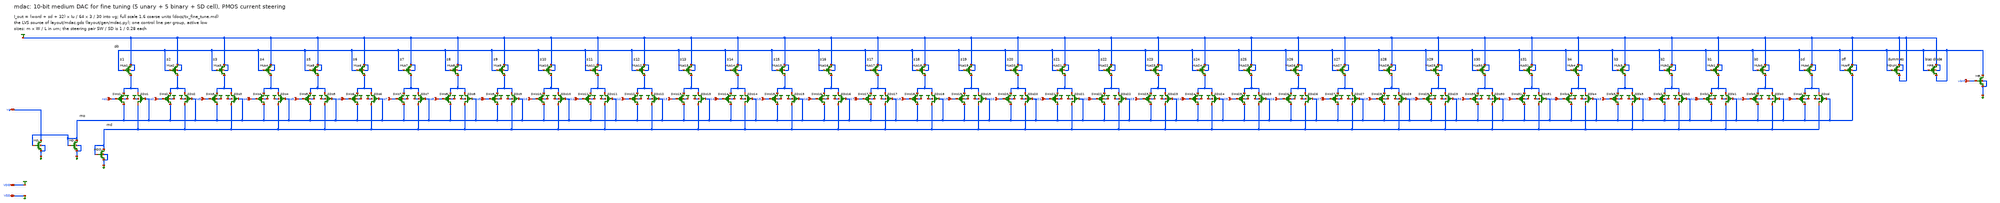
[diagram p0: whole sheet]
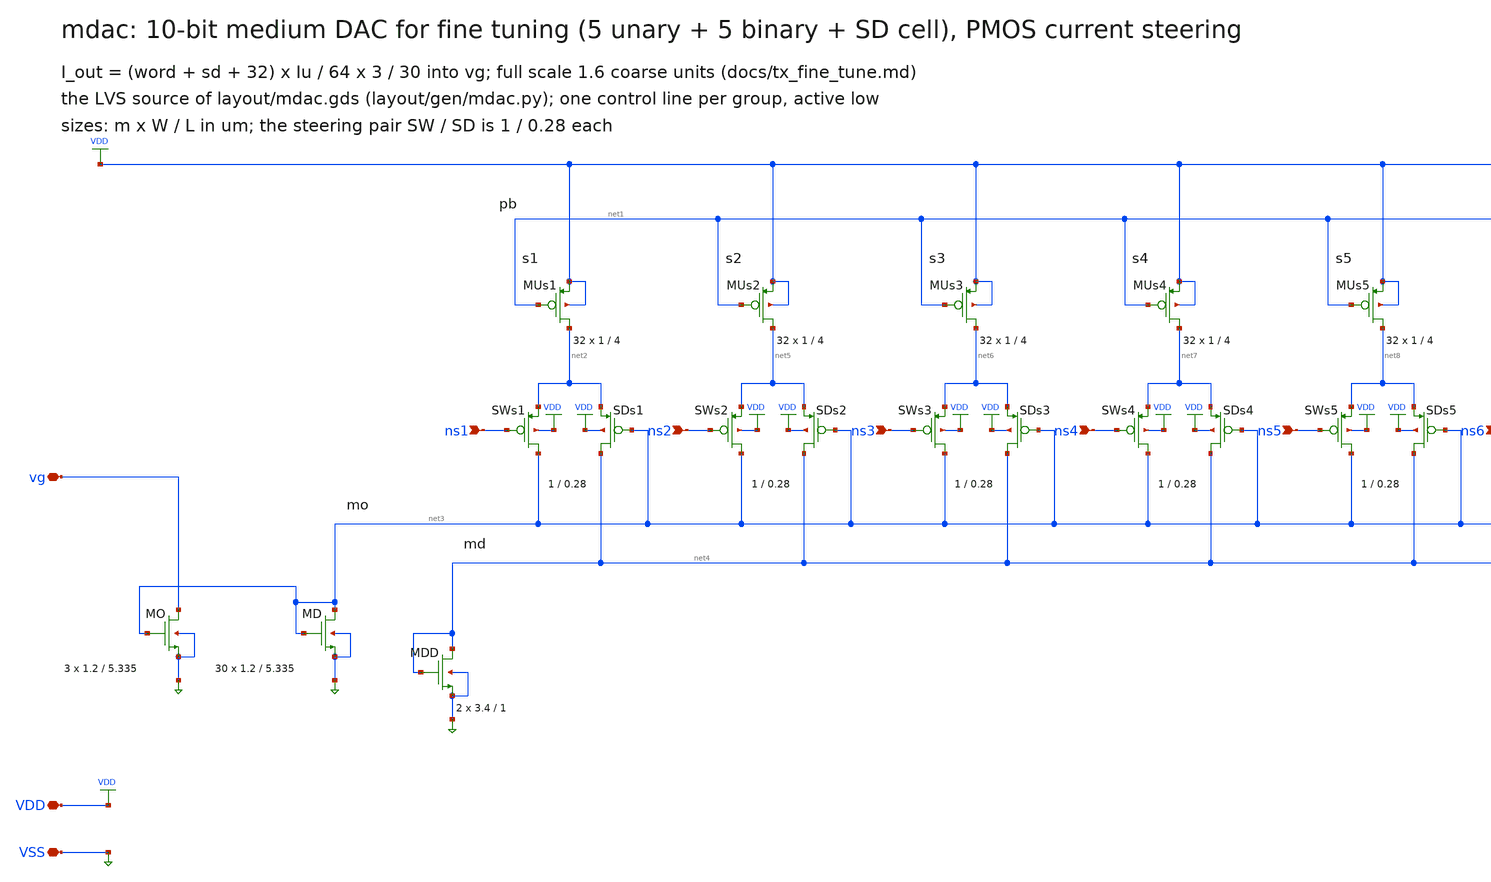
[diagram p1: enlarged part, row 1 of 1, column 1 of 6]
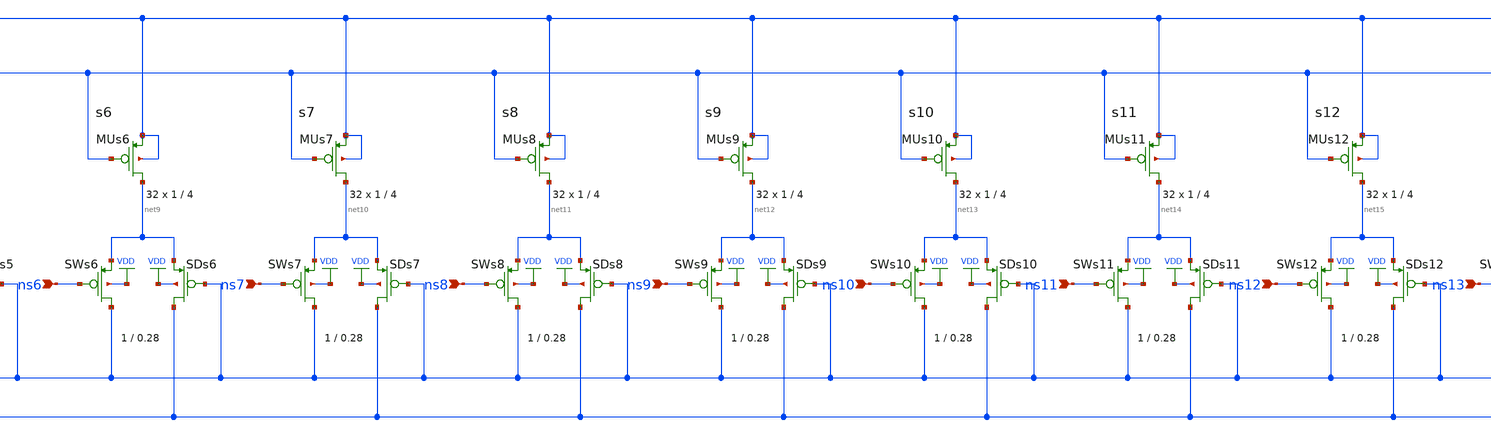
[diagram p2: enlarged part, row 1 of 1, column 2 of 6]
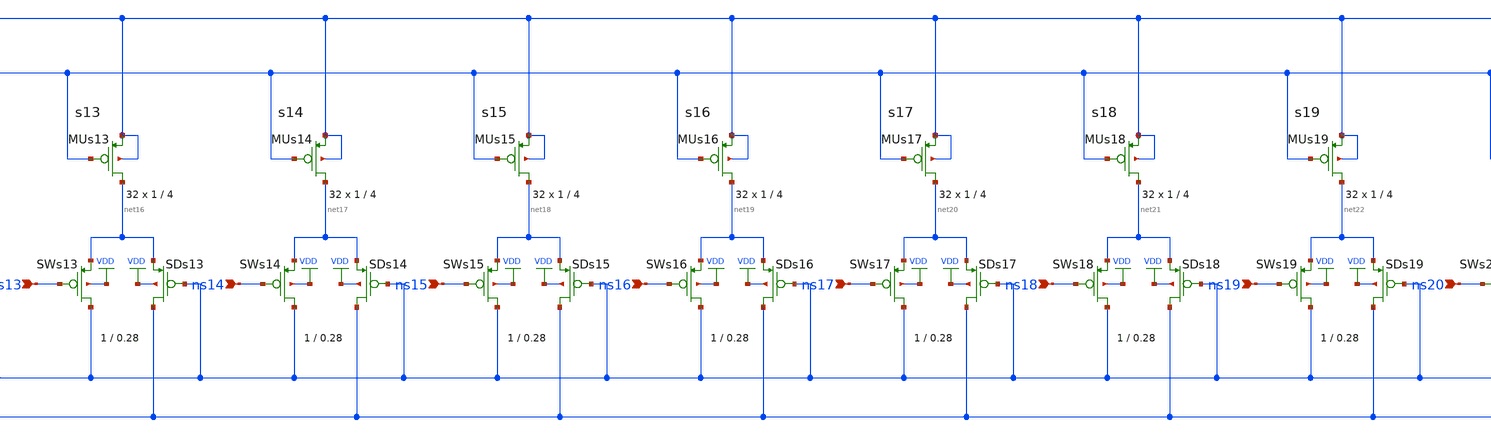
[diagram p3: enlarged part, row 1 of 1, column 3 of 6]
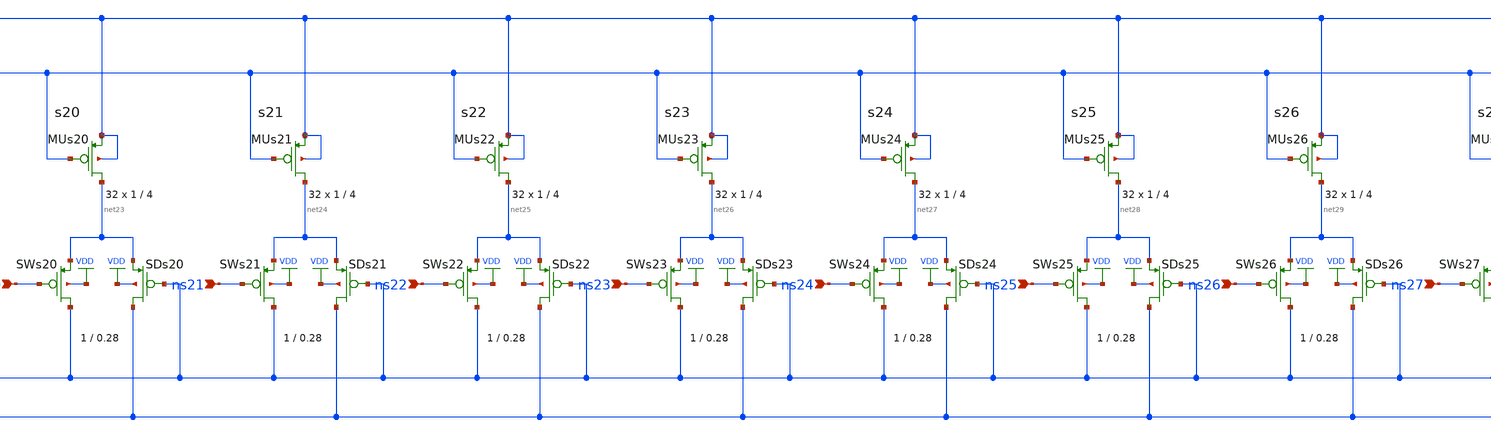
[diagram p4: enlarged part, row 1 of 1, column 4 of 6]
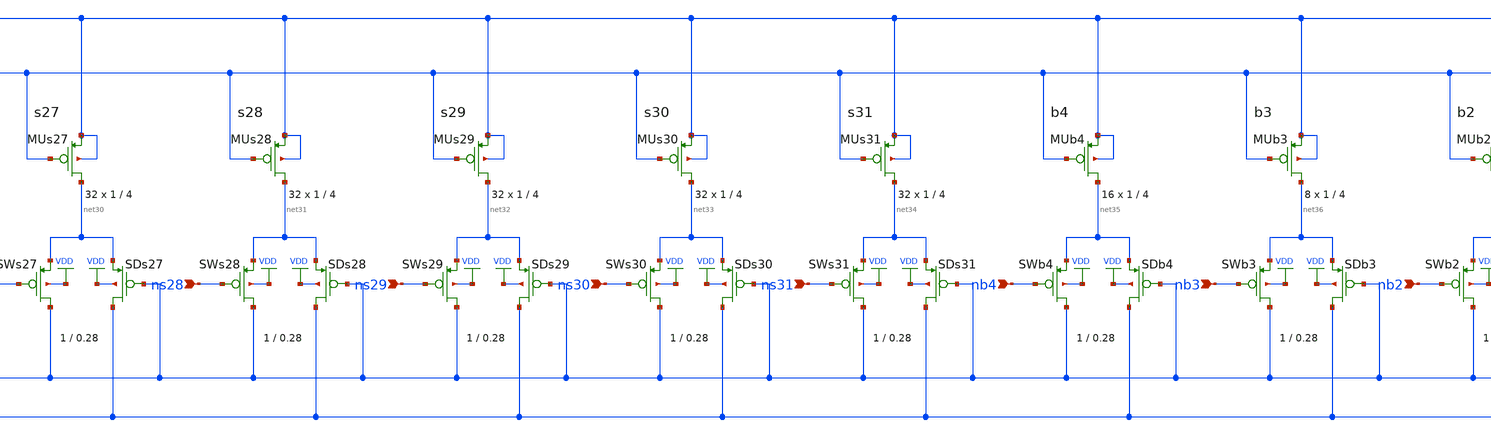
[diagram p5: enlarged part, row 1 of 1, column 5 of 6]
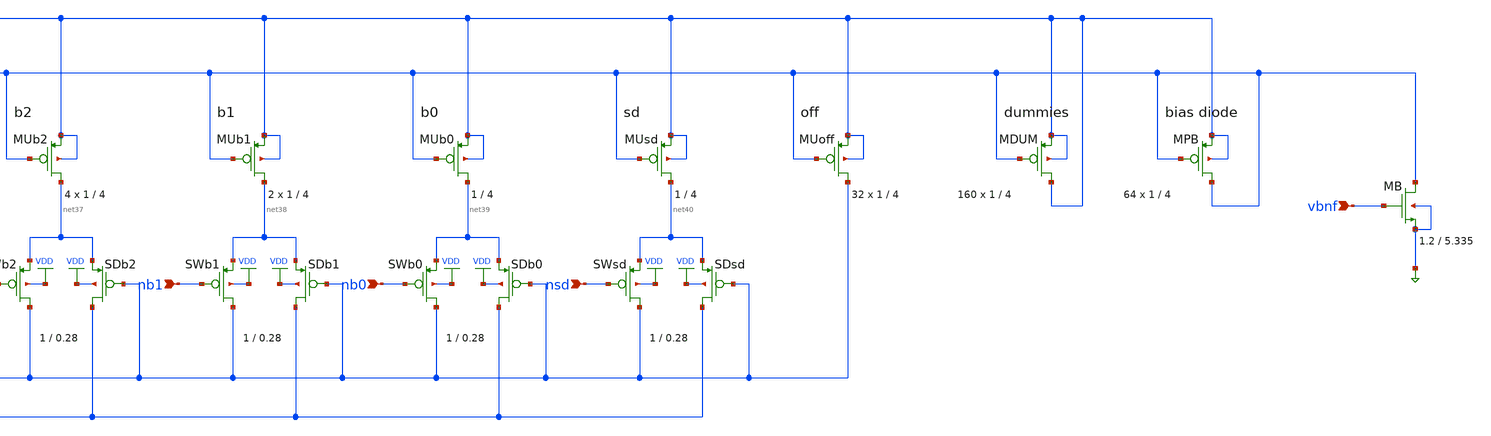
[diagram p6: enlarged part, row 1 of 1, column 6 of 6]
** sch_path: xschem/mdac.sch
**.subckt mdac VDD VSS vg vbnf ns30 ns28 ns26 ns24 ns22 ns20 ns18 ns16 ns14 ns12 ns10 ns8 ns6 ns4
*+ ns2 nb4 nb2 nb0 nsd nb1 nb3 ns1 ns3 ns5 ns7 ns9 ns11 ns13 ns15 ns17 ns19 ns21 ns23 ns25 ns27 ns29 ns31
*.iopin VDD
*.iopin VSS
*.iopin vg
*.ipin vbnf
*.ipin ns30
*.ipin ns28
*.ipin ns26
*.ipin ns24
*.ipin ns22
*.ipin ns20
*.ipin ns18
*.ipin ns16
*.ipin ns14
*.ipin ns12
*.ipin ns10
*.ipin ns8
*.ipin ns6
*.ipin ns4
*.ipin ns2
*.ipin nb4
*.ipin nb2
*.ipin nb0
*.ipin nsd
*.ipin nb1
*.ipin nb3
*.ipin ns1
*.ipin ns3
*.ipin ns5
*.ipin ns7
*.ipin ns9
*.ipin ns11
*.ipin ns13
*.ipin ns15
*.ipin ns17
*.ipin ns19
*.ipin ns21
*.ipin ns23
*.ipin ns25
*.ipin ns27
*.ipin ns29
*.ipin ns31
XMUs1 net2 net1 VDD VDD pfet_03v3 L=4.0u W=1.0u nf=1 ad=0.5p as=0.5p pd=3.0u ps=3.0u nrd=0 nrs=0
+ sa=0 sb=0 sd=0 m=32
XSWs1 net3 ns1 net2 VDD pfet_03v3 L=0.28u W=1.0u nf=1 ad=0.5p as=0.5p pd=3.0u ps=3.0u nrd=0 nrs=0
+ sa=0 sb=0 sd=0 m=1
XSDs1 net4 net3 net2 VDD pfet_03v3 L=0.28u W=1.0u nf=1 ad=0.5p as=0.5p pd=3.0u ps=3.0u nrd=0 nrs=0
+ sa=0 sb=0 sd=0 m=1
XMUs2 net5 net1 VDD VDD pfet_03v3 L=4.0u W=1.0u nf=1 ad=0.5p as=0.5p pd=3.0u ps=3.0u nrd=0 nrs=0
+ sa=0 sb=0 sd=0 m=32
XSWs2 net3 ns2 net5 VDD pfet_03v3 L=0.28u W=1.0u nf=1 ad=0.5p as=0.5p pd=3.0u ps=3.0u nrd=0 nrs=0
+ sa=0 sb=0 sd=0 m=1
XSDs2 net4 net3 net5 VDD pfet_03v3 L=0.28u W=1.0u nf=1 ad=0.5p as=0.5p pd=3.0u ps=3.0u nrd=0 nrs=0
+ sa=0 sb=0 sd=0 m=1
XMUs3 net6 net1 VDD VDD pfet_03v3 L=4.0u W=1.0u nf=1 ad=0.5p as=0.5p pd=3.0u ps=3.0u nrd=0 nrs=0
+ sa=0 sb=0 sd=0 m=32
XSWs3 net3 ns3 net6 VDD pfet_03v3 L=0.28u W=1.0u nf=1 ad=0.5p as=0.5p pd=3.0u ps=3.0u nrd=0 nrs=0
+ sa=0 sb=0 sd=0 m=1
XSDs3 net4 net3 net6 VDD pfet_03v3 L=0.28u W=1.0u nf=1 ad=0.5p as=0.5p pd=3.0u ps=3.0u nrd=0 nrs=0
+ sa=0 sb=0 sd=0 m=1
XMUs4 net7 net1 VDD VDD pfet_03v3 L=4.0u W=1.0u nf=1 ad=0.5p as=0.5p pd=3.0u ps=3.0u nrd=0 nrs=0
+ sa=0 sb=0 sd=0 m=32
XSWs4 net3 ns4 net7 VDD pfet_03v3 L=0.28u W=1.0u nf=1 ad=0.5p as=0.5p pd=3.0u ps=3.0u nrd=0 nrs=0
+ sa=0 sb=0 sd=0 m=1
XSDs4 net4 net3 net7 VDD pfet_03v3 L=0.28u W=1.0u nf=1 ad=0.5p as=0.5p pd=3.0u ps=3.0u nrd=0 nrs=0
+ sa=0 sb=0 sd=0 m=1
XMUs5 net8 net1 VDD VDD pfet_03v3 L=4.0u W=1.0u nf=1 ad=0.5p as=0.5p pd=3.0u ps=3.0u nrd=0 nrs=0
+ sa=0 sb=0 sd=0 m=32
XSWs5 net3 ns5 net8 VDD pfet_03v3 L=0.28u W=1.0u nf=1 ad=0.5p as=0.5p pd=3.0u ps=3.0u nrd=0 nrs=0
+ sa=0 sb=0 sd=0 m=1
XSDs5 net4 net3 net8 VDD pfet_03v3 L=0.28u W=1.0u nf=1 ad=0.5p as=0.5p pd=3.0u ps=3.0u nrd=0 nrs=0
+ sa=0 sb=0 sd=0 m=1
XMUs6 net9 net1 VDD VDD pfet_03v3 L=4.0u W=1.0u nf=1 ad=0.5p as=0.5p pd=3.0u ps=3.0u nrd=0 nrs=0
+ sa=0 sb=0 sd=0 m=32
XSWs6 net3 ns6 net9 VDD pfet_03v3 L=0.28u W=1.0u nf=1 ad=0.5p as=0.5p pd=3.0u ps=3.0u nrd=0 nrs=0
+ sa=0 sb=0 sd=0 m=1
XSDs6 net4 net3 net9 VDD pfet_03v3 L=0.28u W=1.0u nf=1 ad=0.5p as=0.5p pd=3.0u ps=3.0u nrd=0 nrs=0
+ sa=0 sb=0 sd=0 m=1
XMUs7 net10 net1 VDD VDD pfet_03v3 L=4.0u W=1.0u nf=1 ad=0.5p as=0.5p pd=3.0u ps=3.0u nrd=0 nrs=0
+ sa=0 sb=0 sd=0 m=32
XSWs7 net3 ns7 net10 VDD pfet_03v3 L=0.28u W=1.0u nf=1 ad=0.5p as=0.5p pd=3.0u ps=3.0u nrd=0 nrs=0
+ sa=0 sb=0 sd=0 m=1
XSDs7 net4 net3 net10 VDD pfet_03v3 L=0.28u W=1.0u nf=1 ad=0.5p as=0.5p pd=3.0u ps=3.0u nrd=0 nrs=0
+ sa=0 sb=0 sd=0 m=1
XMUs8 net11 net1 VDD VDD pfet_03v3 L=4.0u W=1.0u nf=1 ad=0.5p as=0.5p pd=3.0u ps=3.0u nrd=0 nrs=0
+ sa=0 sb=0 sd=0 m=32
XSWs8 net3 ns8 net11 VDD pfet_03v3 L=0.28u W=1.0u nf=1 ad=0.5p as=0.5p pd=3.0u ps=3.0u nrd=0 nrs=0
+ sa=0 sb=0 sd=0 m=1
XSDs8 net4 net3 net11 VDD pfet_03v3 L=0.28u W=1.0u nf=1 ad=0.5p as=0.5p pd=3.0u ps=3.0u nrd=0 nrs=0
+ sa=0 sb=0 sd=0 m=1
XMUs9 net12 net1 VDD VDD pfet_03v3 L=4.0u W=1.0u nf=1 ad=0.5p as=0.5p pd=3.0u ps=3.0u nrd=0 nrs=0
+ sa=0 sb=0 sd=0 m=32
XSWs9 net3 ns9 net12 VDD pfet_03v3 L=0.28u W=1.0u nf=1 ad=0.5p as=0.5p pd=3.0u ps=3.0u nrd=0 nrs=0
+ sa=0 sb=0 sd=0 m=1
XSDs9 net4 net3 net12 VDD pfet_03v3 L=0.28u W=1.0u nf=1 ad=0.5p as=0.5p pd=3.0u ps=3.0u nrd=0 nrs=0
+ sa=0 sb=0 sd=0 m=1
XMUs10 net13 net1 VDD VDD pfet_03v3 L=4.0u W=1.0u nf=1 ad=0.5p as=0.5p pd=3.0u ps=3.0u nrd=0 nrs=0
+ sa=0 sb=0 sd=0 m=32
XSWs10 net3 ns10 net13 VDD pfet_03v3 L=0.28u W=1.0u nf=1 ad=0.5p as=0.5p pd=3.0u ps=3.0u nrd=0 nrs=0
+ sa=0 sb=0 sd=0 m=1
XSDs10 net4 net3 net13 VDD pfet_03v3 L=0.28u W=1.0u nf=1 ad=0.5p as=0.5p pd=3.0u ps=3.0u nrd=0 nrs=0
+ sa=0 sb=0 sd=0 m=1
XMUs11 net14 net1 VDD VDD pfet_03v3 L=4.0u W=1.0u nf=1 ad=0.5p as=0.5p pd=3.0u ps=3.0u nrd=0 nrs=0
+ sa=0 sb=0 sd=0 m=32
XSWs11 net3 ns11 net14 VDD pfet_03v3 L=0.28u W=1.0u nf=1 ad=0.5p as=0.5p pd=3.0u ps=3.0u nrd=0 nrs=0
+ sa=0 sb=0 sd=0 m=1
XSDs11 net4 net3 net14 VDD pfet_03v3 L=0.28u W=1.0u nf=1 ad=0.5p as=0.5p pd=3.0u ps=3.0u nrd=0 nrs=0
+ sa=0 sb=0 sd=0 m=1
XMUs12 net15 net1 VDD VDD pfet_03v3 L=4.0u W=1.0u nf=1 ad=0.5p as=0.5p pd=3.0u ps=3.0u nrd=0 nrs=0
+ sa=0 sb=0 sd=0 m=32
XSWs12 net3 ns12 net15 VDD pfet_03v3 L=0.28u W=1.0u nf=1 ad=0.5p as=0.5p pd=3.0u ps=3.0u nrd=0 nrs=0
+ sa=0 sb=0 sd=0 m=1
XSDs12 net4 net3 net15 VDD pfet_03v3 L=0.28u W=1.0u nf=1 ad=0.5p as=0.5p pd=3.0u ps=3.0u nrd=0 nrs=0
+ sa=0 sb=0 sd=0 m=1
XMUs13 net16 net1 VDD VDD pfet_03v3 L=4.0u W=1.0u nf=1 ad=0.5p as=0.5p pd=3.0u ps=3.0u nrd=0 nrs=0
+ sa=0 sb=0 sd=0 m=32
XSWs13 net3 ns13 net16 VDD pfet_03v3 L=0.28u W=1.0u nf=1 ad=0.5p as=0.5p pd=3.0u ps=3.0u nrd=0 nrs=0
+ sa=0 sb=0 sd=0 m=1
XSDs13 net4 net3 net16 VDD pfet_03v3 L=0.28u W=1.0u nf=1 ad=0.5p as=0.5p pd=3.0u ps=3.0u nrd=0 nrs=0
+ sa=0 sb=0 sd=0 m=1
XMUs14 net17 net1 VDD VDD pfet_03v3 L=4.0u W=1.0u nf=1 ad=0.5p as=0.5p pd=3.0u ps=3.0u nrd=0 nrs=0
+ sa=0 sb=0 sd=0 m=32
XSWs14 net3 ns14 net17 VDD pfet_03v3 L=0.28u W=1.0u nf=1 ad=0.5p as=0.5p pd=3.0u ps=3.0u nrd=0 nrs=0
+ sa=0 sb=0 sd=0 m=1
XSDs14 net4 net3 net17 VDD pfet_03v3 L=0.28u W=1.0u nf=1 ad=0.5p as=0.5p pd=3.0u ps=3.0u nrd=0 nrs=0
+ sa=0 sb=0 sd=0 m=1
XMUs15 net18 net1 VDD VDD pfet_03v3 L=4.0u W=1.0u nf=1 ad=0.5p as=0.5p pd=3.0u ps=3.0u nrd=0 nrs=0
+ sa=0 sb=0 sd=0 m=32
XSWs15 net3 ns15 net18 VDD pfet_03v3 L=0.28u W=1.0u nf=1 ad=0.5p as=0.5p pd=3.0u ps=3.0u nrd=0 nrs=0
+ sa=0 sb=0 sd=0 m=1
XSDs15 net4 net3 net18 VDD pfet_03v3 L=0.28u W=1.0u nf=1 ad=0.5p as=0.5p pd=3.0u ps=3.0u nrd=0 nrs=0
+ sa=0 sb=0 sd=0 m=1
XMUs16 net19 net1 VDD VDD pfet_03v3 L=4.0u W=1.0u nf=1 ad=0.5p as=0.5p pd=3.0u ps=3.0u nrd=0 nrs=0
+ sa=0 sb=0 sd=0 m=32
XSWs16 net3 ns16 net19 VDD pfet_03v3 L=0.28u W=1.0u nf=1 ad=0.5p as=0.5p pd=3.0u ps=3.0u nrd=0 nrs=0
+ sa=0 sb=0 sd=0 m=1
XSDs16 net4 net3 net19 VDD pfet_03v3 L=0.28u W=1.0u nf=1 ad=0.5p as=0.5p pd=3.0u ps=3.0u nrd=0 nrs=0
+ sa=0 sb=0 sd=0 m=1
XMUs17 net20 net1 VDD VDD pfet_03v3 L=4.0u W=1.0u nf=1 ad=0.5p as=0.5p pd=3.0u ps=3.0u nrd=0 nrs=0
+ sa=0 sb=0 sd=0 m=32
XSWs17 net3 ns17 net20 VDD pfet_03v3 L=0.28u W=1.0u nf=1 ad=0.5p as=0.5p pd=3.0u ps=3.0u nrd=0 nrs=0
+ sa=0 sb=0 sd=0 m=1
XSDs17 net4 net3 net20 VDD pfet_03v3 L=0.28u W=1.0u nf=1 ad=0.5p as=0.5p pd=3.0u ps=3.0u nrd=0 nrs=0
+ sa=0 sb=0 sd=0 m=1
XMUs18 net21 net1 VDD VDD pfet_03v3 L=4.0u W=1.0u nf=1 ad=0.5p as=0.5p pd=3.0u ps=3.0u nrd=0 nrs=0
+ sa=0 sb=0 sd=0 m=32
XSWs18 net3 ns18 net21 VDD pfet_03v3 L=0.28u W=1.0u nf=1 ad=0.5p as=0.5p pd=3.0u ps=3.0u nrd=0 nrs=0
+ sa=0 sb=0 sd=0 m=1
XSDs18 net4 net3 net21 VDD pfet_03v3 L=0.28u W=1.0u nf=1 ad=0.5p as=0.5p pd=3.0u ps=3.0u nrd=0 nrs=0
+ sa=0 sb=0 sd=0 m=1
XMUs19 net22 net1 VDD VDD pfet_03v3 L=4.0u W=1.0u nf=1 ad=0.5p as=0.5p pd=3.0u ps=3.0u nrd=0 nrs=0
+ sa=0 sb=0 sd=0 m=32
XSWs19 net3 ns19 net22 VDD pfet_03v3 L=0.28u W=1.0u nf=1 ad=0.5p as=0.5p pd=3.0u ps=3.0u nrd=0 nrs=0
+ sa=0 sb=0 sd=0 m=1
XSDs19 net4 net3 net22 VDD pfet_03v3 L=0.28u W=1.0u nf=1 ad=0.5p as=0.5p pd=3.0u ps=3.0u nrd=0 nrs=0
+ sa=0 sb=0 sd=0 m=1
XMUs20 net23 net1 VDD VDD pfet_03v3 L=4.0u W=1.0u nf=1 ad=0.5p as=0.5p pd=3.0u ps=3.0u nrd=0 nrs=0
+ sa=0 sb=0 sd=0 m=32
XSWs20 net3 ns20 net23 VDD pfet_03v3 L=0.28u W=1.0u nf=1 ad=0.5p as=0.5p pd=3.0u ps=3.0u nrd=0 nrs=0
+ sa=0 sb=0 sd=0 m=1
XSDs20 net4 net3 net23 VDD pfet_03v3 L=0.28u W=1.0u nf=1 ad=0.5p as=0.5p pd=3.0u ps=3.0u nrd=0 nrs=0
+ sa=0 sb=0 sd=0 m=1
XMUs21 net24 net1 VDD VDD pfet_03v3 L=4.0u W=1.0u nf=1 ad=0.5p as=0.5p pd=3.0u ps=3.0u nrd=0 nrs=0
+ sa=0 sb=0 sd=0 m=32
XSWs21 net3 ns21 net24 VDD pfet_03v3 L=0.28u W=1.0u nf=1 ad=0.5p as=0.5p pd=3.0u ps=3.0u nrd=0 nrs=0
+ sa=0 sb=0 sd=0 m=1
XSDs21 net4 net3 net24 VDD pfet_03v3 L=0.28u W=1.0u nf=1 ad=0.5p as=0.5p pd=3.0u ps=3.0u nrd=0 nrs=0
+ sa=0 sb=0 sd=0 m=1
XMUs22 net25 net1 VDD VDD pfet_03v3 L=4.0u W=1.0u nf=1 ad=0.5p as=0.5p pd=3.0u ps=3.0u nrd=0 nrs=0
+ sa=0 sb=0 sd=0 m=32
XSWs22 net3 ns22 net25 VDD pfet_03v3 L=0.28u W=1.0u nf=1 ad=0.5p as=0.5p pd=3.0u ps=3.0u nrd=0 nrs=0
+ sa=0 sb=0 sd=0 m=1
XSDs22 net4 net3 net25 VDD pfet_03v3 L=0.28u W=1.0u nf=1 ad=0.5p as=0.5p pd=3.0u ps=3.0u nrd=0 nrs=0
+ sa=0 sb=0 sd=0 m=1
XMUs23 net26 net1 VDD VDD pfet_03v3 L=4.0u W=1.0u nf=1 ad=0.5p as=0.5p pd=3.0u ps=3.0u nrd=0 nrs=0
+ sa=0 sb=0 sd=0 m=32
XSWs23 net3 ns23 net26 VDD pfet_03v3 L=0.28u W=1.0u nf=1 ad=0.5p as=0.5p pd=3.0u ps=3.0u nrd=0 nrs=0
+ sa=0 sb=0 sd=0 m=1
XSDs23 net4 net3 net26 VDD pfet_03v3 L=0.28u W=1.0u nf=1 ad=0.5p as=0.5p pd=3.0u ps=3.0u nrd=0 nrs=0
+ sa=0 sb=0 sd=0 m=1
XMUs24 net27 net1 VDD VDD pfet_03v3 L=4.0u W=1.0u nf=1 ad=0.5p as=0.5p pd=3.0u ps=3.0u nrd=0 nrs=0
+ sa=0 sb=0 sd=0 m=32
XSWs24 net3 ns24 net27 VDD pfet_03v3 L=0.28u W=1.0u nf=1 ad=0.5p as=0.5p pd=3.0u ps=3.0u nrd=0 nrs=0
+ sa=0 sb=0 sd=0 m=1
XSDs24 net4 net3 net27 VDD pfet_03v3 L=0.28u W=1.0u nf=1 ad=0.5p as=0.5p pd=3.0u ps=3.0u nrd=0 nrs=0
+ sa=0 sb=0 sd=0 m=1
XMUs25 net28 net1 VDD VDD pfet_03v3 L=4.0u W=1.0u nf=1 ad=0.5p as=0.5p pd=3.0u ps=3.0u nrd=0 nrs=0
+ sa=0 sb=0 sd=0 m=32
XSWs25 net3 ns25 net28 VDD pfet_03v3 L=0.28u W=1.0u nf=1 ad=0.5p as=0.5p pd=3.0u ps=3.0u nrd=0 nrs=0
+ sa=0 sb=0 sd=0 m=1
XSDs25 net4 net3 net28 VDD pfet_03v3 L=0.28u W=1.0u nf=1 ad=0.5p as=0.5p pd=3.0u ps=3.0u nrd=0 nrs=0
+ sa=0 sb=0 sd=0 m=1
XMUs26 net29 net1 VDD VDD pfet_03v3 L=4.0u W=1.0u nf=1 ad=0.5p as=0.5p pd=3.0u ps=3.0u nrd=0 nrs=0
+ sa=0 sb=0 sd=0 m=32
XSWs26 net3 ns26 net29 VDD pfet_03v3 L=0.28u W=1.0u nf=1 ad=0.5p as=0.5p pd=3.0u ps=3.0u nrd=0 nrs=0
+ sa=0 sb=0 sd=0 m=1
XSDs26 net4 net3 net29 VDD pfet_03v3 L=0.28u W=1.0u nf=1 ad=0.5p as=0.5p pd=3.0u ps=3.0u nrd=0 nrs=0
+ sa=0 sb=0 sd=0 m=1
XMUs27 net30 net1 VDD VDD pfet_03v3 L=4.0u W=1.0u nf=1 ad=0.5p as=0.5p pd=3.0u ps=3.0u nrd=0 nrs=0
+ sa=0 sb=0 sd=0 m=32
XSWs27 net3 ns27 net30 VDD pfet_03v3 L=0.28u W=1.0u nf=1 ad=0.5p as=0.5p pd=3.0u ps=3.0u nrd=0 nrs=0
+ sa=0 sb=0 sd=0 m=1
XSDs27 net4 net3 net30 VDD pfet_03v3 L=0.28u W=1.0u nf=1 ad=0.5p as=0.5p pd=3.0u ps=3.0u nrd=0 nrs=0
+ sa=0 sb=0 sd=0 m=1
XMUs28 net31 net1 VDD VDD pfet_03v3 L=4.0u W=1.0u nf=1 ad=0.5p as=0.5p pd=3.0u ps=3.0u nrd=0 nrs=0
+ sa=0 sb=0 sd=0 m=32
XSWs28 net3 ns28 net31 VDD pfet_03v3 L=0.28u W=1.0u nf=1 ad=0.5p as=0.5p pd=3.0u ps=3.0u nrd=0 nrs=0
+ sa=0 sb=0 sd=0 m=1
XSDs28 net4 net3 net31 VDD pfet_03v3 L=0.28u W=1.0u nf=1 ad=0.5p as=0.5p pd=3.0u ps=3.0u nrd=0 nrs=0
+ sa=0 sb=0 sd=0 m=1
XMUs29 net32 net1 VDD VDD pfet_03v3 L=4.0u W=1.0u nf=1 ad=0.5p as=0.5p pd=3.0u ps=3.0u nrd=0 nrs=0
+ sa=0 sb=0 sd=0 m=32
XSWs29 net3 ns29 net32 VDD pfet_03v3 L=0.28u W=1.0u nf=1 ad=0.5p as=0.5p pd=3.0u ps=3.0u nrd=0 nrs=0
+ sa=0 sb=0 sd=0 m=1
XSDs29 net4 net3 net32 VDD pfet_03v3 L=0.28u W=1.0u nf=1 ad=0.5p as=0.5p pd=3.0u ps=3.0u nrd=0 nrs=0
+ sa=0 sb=0 sd=0 m=1
XMUs30 net33 net1 VDD VDD pfet_03v3 L=4.0u W=1.0u nf=1 ad=0.5p as=0.5p pd=3.0u ps=3.0u nrd=0 nrs=0
+ sa=0 sb=0 sd=0 m=32
XSWs30 net3 ns30 net33 VDD pfet_03v3 L=0.28u W=1.0u nf=1 ad=0.5p as=0.5p pd=3.0u ps=3.0u nrd=0 nrs=0
+ sa=0 sb=0 sd=0 m=1
XSDs30 net4 net3 net33 VDD pfet_03v3 L=0.28u W=1.0u nf=1 ad=0.5p as=0.5p pd=3.0u ps=3.0u nrd=0 nrs=0
+ sa=0 sb=0 sd=0 m=1
XMUs31 net34 net1 VDD VDD pfet_03v3 L=4.0u W=1.0u nf=1 ad=0.5p as=0.5p pd=3.0u ps=3.0u nrd=0 nrs=0
+ sa=0 sb=0 sd=0 m=32
XSWs31 net3 ns31 net34 VDD pfet_03v3 L=0.28u W=1.0u nf=1 ad=0.5p as=0.5p pd=3.0u ps=3.0u nrd=0 nrs=0
+ sa=0 sb=0 sd=0 m=1
XSDs31 net4 net3 net34 VDD pfet_03v3 L=0.28u W=1.0u nf=1 ad=0.5p as=0.5p pd=3.0u ps=3.0u nrd=0 nrs=0
+ sa=0 sb=0 sd=0 m=1
XMUb4 net35 net1 VDD VDD pfet_03v3 L=4.0u W=1.0u nf=1 ad=0.5p as=0.5p pd=3.0u ps=3.0u nrd=0 nrs=0
+ sa=0 sb=0 sd=0 m=16
XSWb4 net3 nb4 net35 VDD pfet_03v3 L=0.28u W=1.0u nf=1 ad=0.5p as=0.5p pd=3.0u ps=3.0u nrd=0 nrs=0
+ sa=0 sb=0 sd=0 m=1
XSDb4 net4 net3 net35 VDD pfet_03v3 L=0.28u W=1.0u nf=1 ad=0.5p as=0.5p pd=3.0u ps=3.0u nrd=0 nrs=0
+ sa=0 sb=0 sd=0 m=1
XMUb3 net36 net1 VDD VDD pfet_03v3 L=4.0u W=1.0u nf=1 ad=0.5p as=0.5p pd=3.0u ps=3.0u nrd=0 nrs=0
+ sa=0 sb=0 sd=0 m=8
XSWb3 net3 nb3 net36 VDD pfet_03v3 L=0.28u W=1.0u nf=1 ad=0.5p as=0.5p pd=3.0u ps=3.0u nrd=0 nrs=0
+ sa=0 sb=0 sd=0 m=1
XSDb3 net4 net3 net36 VDD pfet_03v3 L=0.28u W=1.0u nf=1 ad=0.5p as=0.5p pd=3.0u ps=3.0u nrd=0 nrs=0
+ sa=0 sb=0 sd=0 m=1
XMUb2 net37 net1 VDD VDD pfet_03v3 L=4.0u W=1.0u nf=1 ad=0.5p as=0.5p pd=3.0u ps=3.0u nrd=0 nrs=0
+ sa=0 sb=0 sd=0 m=4
XSWb2 net3 nb2 net37 VDD pfet_03v3 L=0.28u W=1.0u nf=1 ad=0.5p as=0.5p pd=3.0u ps=3.0u nrd=0 nrs=0
+ sa=0 sb=0 sd=0 m=1
XSDb2 net4 net3 net37 VDD pfet_03v3 L=0.28u W=1.0u nf=1 ad=0.5p as=0.5p pd=3.0u ps=3.0u nrd=0 nrs=0
+ sa=0 sb=0 sd=0 m=1
XMUb1 net38 net1 VDD VDD pfet_03v3 L=4.0u W=1.0u nf=1 ad=0.5p as=0.5p pd=3.0u ps=3.0u nrd=0 nrs=0
+ sa=0 sb=0 sd=0 m=2
XSWb1 net3 nb1 net38 VDD pfet_03v3 L=0.28u W=1.0u nf=1 ad=0.5p as=0.5p pd=3.0u ps=3.0u nrd=0 nrs=0
+ sa=0 sb=0 sd=0 m=1
XSDb1 net4 net3 net38 VDD pfet_03v3 L=0.28u W=1.0u nf=1 ad=0.5p as=0.5p pd=3.0u ps=3.0u nrd=0 nrs=0
+ sa=0 sb=0 sd=0 m=1
XMUb0 net39 net1 VDD VDD pfet_03v3 L=4.0u W=1.0u nf=1 ad=0.5p as=0.5p pd=3.0u ps=3.0u nrd=0 nrs=0
+ sa=0 sb=0 sd=0 m=1
XSWb0 net3 nb0 net39 VDD pfet_03v3 L=0.28u W=1.0u nf=1 ad=0.5p as=0.5p pd=3.0u ps=3.0u nrd=0 nrs=0
+ sa=0 sb=0 sd=0 m=1
XSDb0 net4 net3 net39 VDD pfet_03v3 L=0.28u W=1.0u nf=1 ad=0.5p as=0.5p pd=3.0u ps=3.0u nrd=0 nrs=0
+ sa=0 sb=0 sd=0 m=1
XMUsd net40 net1 VDD VDD pfet_03v3 L=4.0u W=1.0u nf=1 ad=0.5p as=0.5p pd=3.0u ps=3.0u nrd=0 nrs=0
+ sa=0 sb=0 sd=0 m=1
XSWsd net3 nsd net40 VDD pfet_03v3 L=0.28u W=1.0u nf=1 ad=0.5p as=0.5p pd=3.0u ps=3.0u nrd=0 nrs=0
+ sa=0 sb=0 sd=0 m=1
XSDsd net4 net3 net40 VDD pfet_03v3 L=0.28u W=1.0u nf=1 ad=0.5p as=0.5p pd=3.0u ps=3.0u nrd=0 nrs=0
+ sa=0 sb=0 sd=0 m=1
XMUoff net3 net1 VDD VDD pfet_03v3 L=4.0u W=1.0u nf=1 ad=0.5p as=0.5p pd=3.0u ps=3.0u nrd=0 nrs=0
+ sa=0 sb=0 sd=0 m=32
XMDUM VDD net1 VDD VDD pfet_03v3 L=4.0u W=1.0u nf=1 ad=0.5p as=0.5p pd=3.0u ps=3.0u nrd=0 nrs=0 sa=0
+ sb=0 sd=0 m=160
XMPB net1 net1 VDD VDD pfet_03v3 L=4.0u W=1.0u nf=1 ad=0.5p as=0.5p pd=3.0u ps=3.0u nrd=0 nrs=0 sa=0
+ sb=0 sd=0 m=64
XMB net1 vbnf VSS VSS nfet_03v3 L=5.335u W=1.2u nf=1 ad=0.6p as=0.6p pd=3.4u ps=3.4u nrd=0 nrs=0
+ sa=0 sb=0 sd=0 m=1
XMD net3 net3 VSS VSS nfet_03v3 L=5.335u W=1.2u nf=1 ad=0.6p as=0.6p pd=3.4u ps=3.4u nrd=0 nrs=0
+ sa=0 sb=0 sd=0 m=30
XMO vg net3 VSS VSS nfet_03v3 L=5.335u W=1.2u nf=1 ad=0.6p as=0.6p pd=3.4u ps=3.4u nrd=0 nrs=0 sa=0
+ sb=0 sd=0 m=3
XMDD net4 net4 VSS VSS nfet_03v3 L=1.0u W=3.4u nf=1 ad=1.7p as=1.7p pd=7.8u ps=7.8u nrd=0 nrs=0 sa=0
+ sb=0 sd=0 m=2
**.ends
.end
